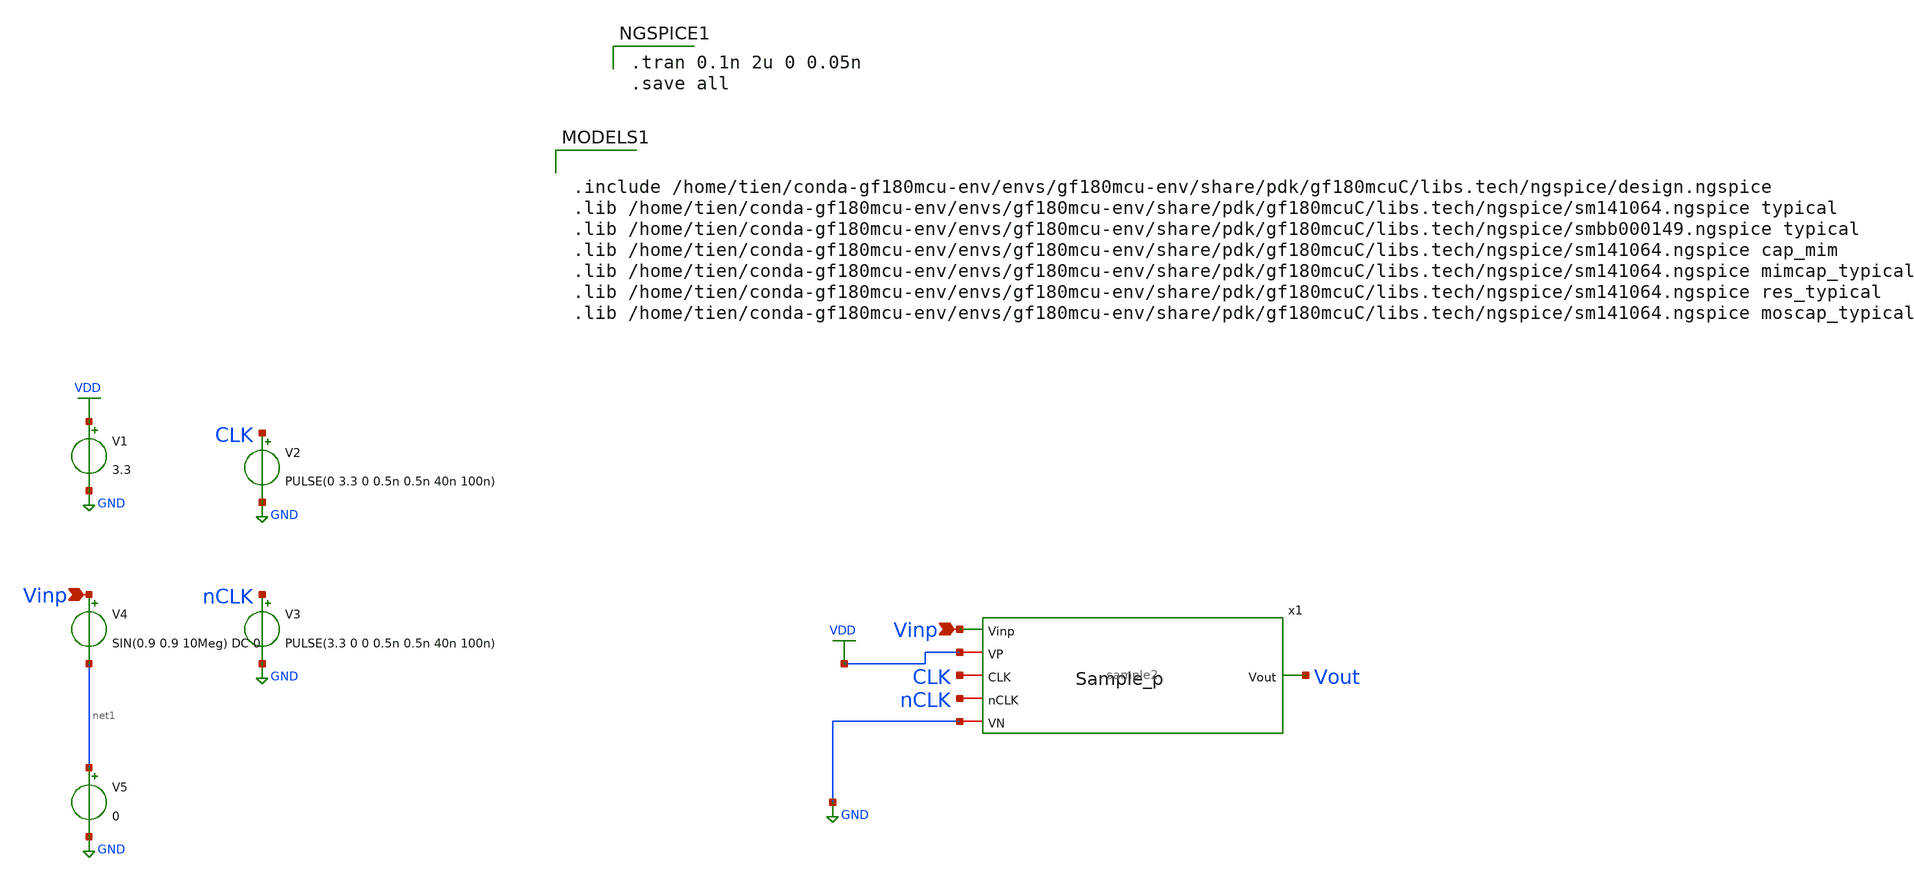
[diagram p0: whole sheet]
** sch_path: Sample and Hold/sa2.sch
**.subckt sa2 Vinp Vinp
*.ipin Vinp
*.ipin Vinp
V1 VDD GND 3.3
V2 CLK GND PULSE(0 3.3 0 0.5n 0.5n 40n 100n)

V3 nCLK GND PULSE(3.3 0 0 0.5n 0.5n 40n 100n)

V4 Vinp net1 SIN(0.9 0.9 10Meg) DC 0
V5 net1 GND 0
x1 VDD CLK Vout nCLK Vinp GND sample2
**** begin user architecture code

.tran 0.1n 2u 0 0.05n
.save all



.include /home/tien/conda-gf180mcu-env/envs/gf180mcu-env/share/pdk/gf180mcuC/libs.tech/ngspice/design.ngspice
.lib /home/tien/conda-gf180mcu-env/envs/gf180mcu-env/share/pdk/gf180mcuC/libs.tech/ngspice/sm141064.ngspice typical
.lib /home/tien/conda-gf180mcu-env/envs/gf180mcu-env/share/pdk/gf180mcuC/libs.tech/ngspice/smbb000149.ngspice typical
.lib /home/tien/conda-gf180mcu-env/envs/gf180mcu-env/share/pdk/gf180mcuC/libs.tech/ngspice/sm141064.ngspice cap_mim
.lib /home/tien/conda-gf180mcu-env/envs/gf180mcu-env/share/pdk/gf180mcuC/libs.tech/ngspice/sm141064.ngspice mimcap_typical
.lib /home/tien/conda-gf180mcu-env/envs/gf180mcu-env/share/pdk/gf180mcuC/libs.tech/ngspice/sm141064.ngspice res_typical
.lib /home/tien/conda-gf180mcu-env/envs/gf180mcu-env/share/pdk/gf180mcuC/libs.tech/ngspice/sm141064.ngspice moscap_typical

**** end user architecture code
**.ends
.GLOBAL VDD
.GLOBAL GND
.end
